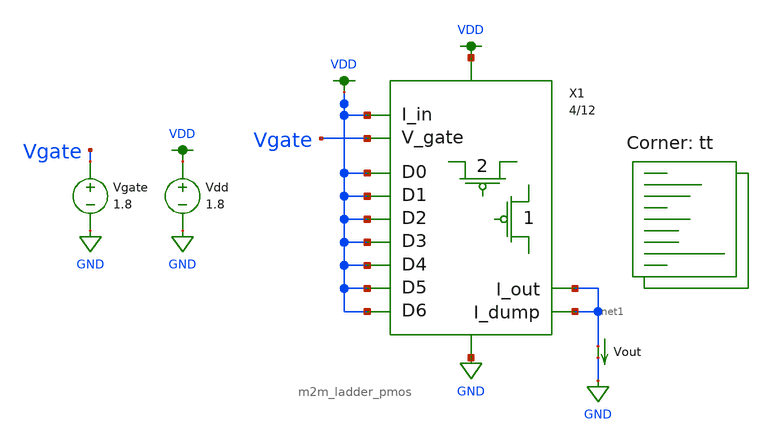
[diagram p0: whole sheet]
** sch_path: dac/schematic/m2m_ladder_isat_tb.sch
**.subckt m2m_ladder_isat_tb
Vdd VDD GND 1.8
Vgate Vgate GND 1.8
Vout net1 GND 0
.save i(vout)
X1 VDD GND VDD VDD VDD VDD VDD VDD VDD Vgate VDD net1 net1 m2m_ladder_pmos u_w=4 u_l=12
**** begin user architecture code
.lib $::SKYWATER_MODELS/sky130.lib.spice tt

.control
  set wr_vecnames
  set wr_singlescale
  dc Vgate 0 1.8 0.01
  wrdata ~/documents/git/madvlsi/dac/build/m2m_ladder_isat/m2m_ladder_isat_tb.txt i(Vout)
.endc

**** end user architecture code
**.ends
.GLOBAL GND
.GLOBAL VDD
.end
